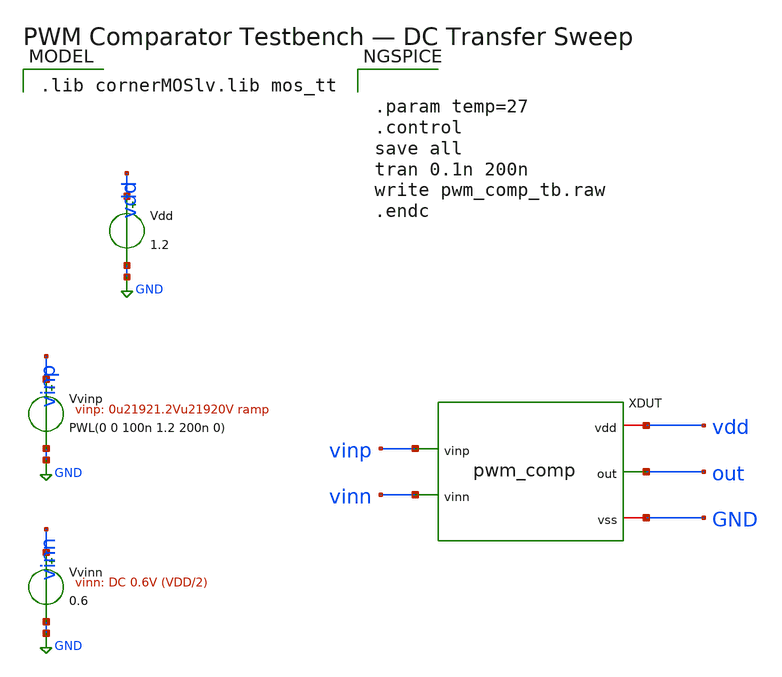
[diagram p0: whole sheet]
** sch_path: xschem/pwm_comp_tb.sch
**.subckt pwm_comp_tb
XDUT vinp vinn out vdd GND pwm_comp
Vdd vdd GND 1.2
Vvinp vinp GND PWL(0 0 100n 1.2 200n 0)
Vvinn vinn GND 0.6
**** begin user architecture code
 .lib cornerMOSlv.lib mos_tt



.param temp=27
.control
save all
tran 0.1n 200n
write pwm_comp_tb.raw
.endc


**** end user architecture code
**.ends

* expanding   symbol:  pwm_comp.sym # of pins=5
** sym_path: xschem/pwm_comp.sym
** sch_path: xschem/pwm_comp.sch
.subckt pwm_comp vinp vinn out vdd vss
*.iopin vdd
*.iopin vss
*.ipin vinp
*.ipin vinn
*.opin out
XXM3 mirr mirr vdd vdd sg13_lv_pmos w=2e-6 l=0.5e-6 ng=1 m=1 mm_ok=1
XXM4 ota_o mirr vdd vdd sg13_lv_pmos w=2e-6 l=0.5e-6 ng=1 m=1 mm_ok=1
XXM1 mirr vinp tail vss sg13_lv_nmos w=4e-6 l=0.5e-6 ng=1 m=1 mm_ok=1
XXM2 ota_o vinn tail vss sg13_lv_nmos w=4e-6 l=0.5e-6 ng=1 m=1 mm_ok=1
XXM5 tail tail vss vss sg13_lv_nmos w=2e-6 l=0.5e-6 ng=1 m=1 mm_ok=1
XXM7 out ota_o vdd vdd sg13_lv_pmos w=1e-6 l=0.13e-6 ng=1 m=1 mm_ok=1
XXM6 out ota_o vss vss sg13_lv_nmos w=0.5e-6 l=0.13e-6 ng=1 m=1 mm_ok=1
.ends

.GLOBAL GND
.end
